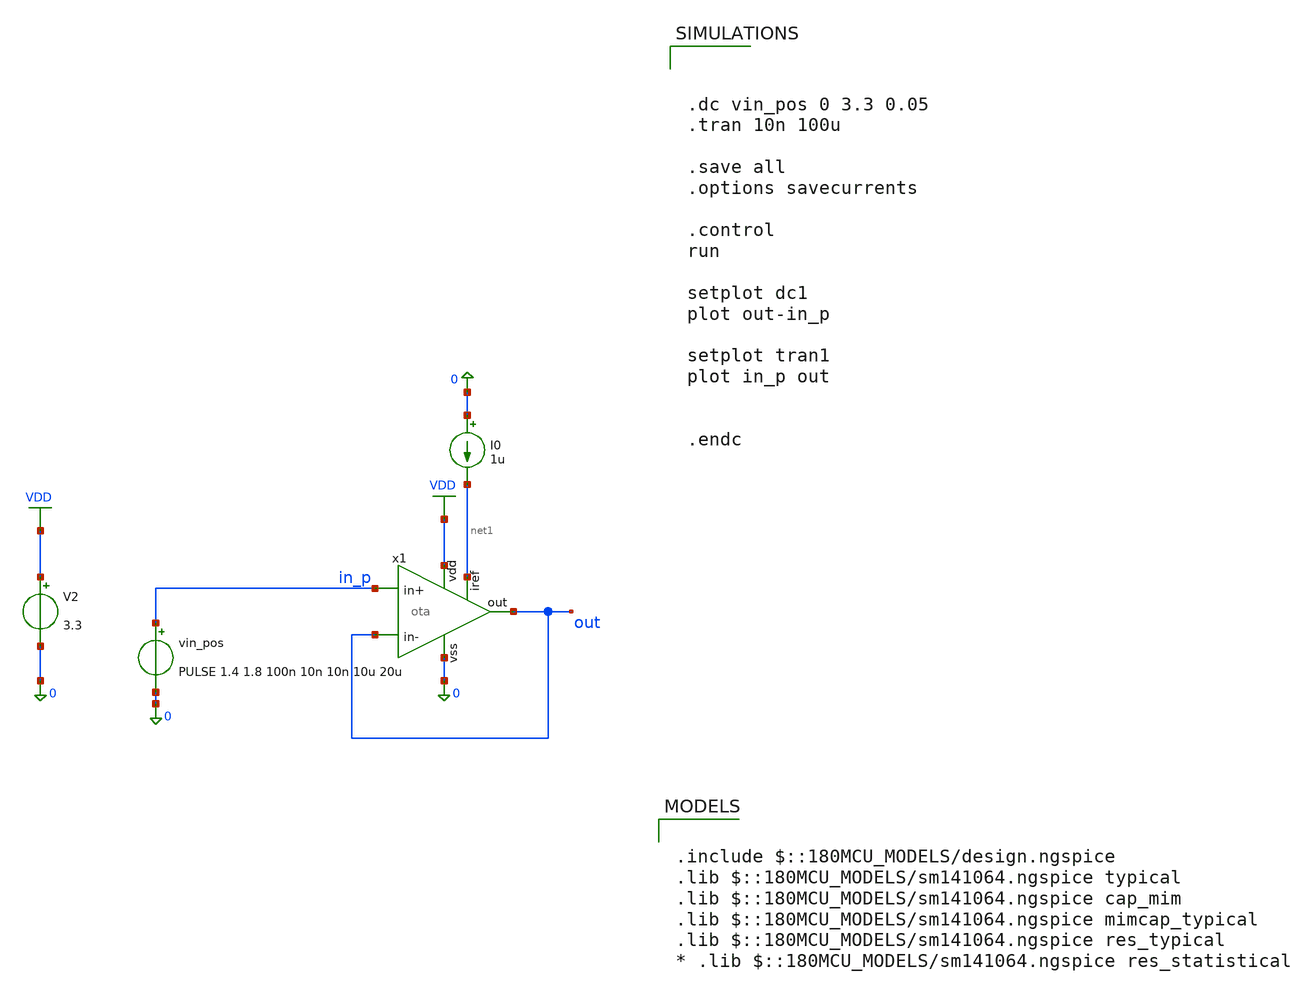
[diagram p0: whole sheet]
** sch_path: General/ADC/OTA/ota_tb_buffer.sch
**.subckt ota_tb_buffer
vin_pos in_p 0 PULSE 1.4 1.8 100n 10n 10n 10u 20u
V2 VDD 0 3.3
.save i(v2)
I0 0 net1 1u
x1 out out in_p VDD 0 net1 ota
**** begin user architecture code

.include $::180MCU_MODELS/design.ngspice
.lib $::180MCU_MODELS/sm141064.ngspice typical
.lib $::180MCU_MODELS/sm141064.ngspice cap_mim
.lib $::180MCU_MODELS/sm141064.ngspice mimcap_typical
.lib $::180MCU_MODELS/sm141064.ngspice res_typical
* .lib $::180MCU_MODELS/sm141064.ngspice res_statistical




.dc vin_pos 0 3.3 0.05
.tran 10n 100u

.save all
.options savecurrents

.control
run

setplot dc1
plot out-in_p

setplot tran1
plot in_p out


.endc


**** end user architecture code
**.ends
.GLOBAL VDD
.end
